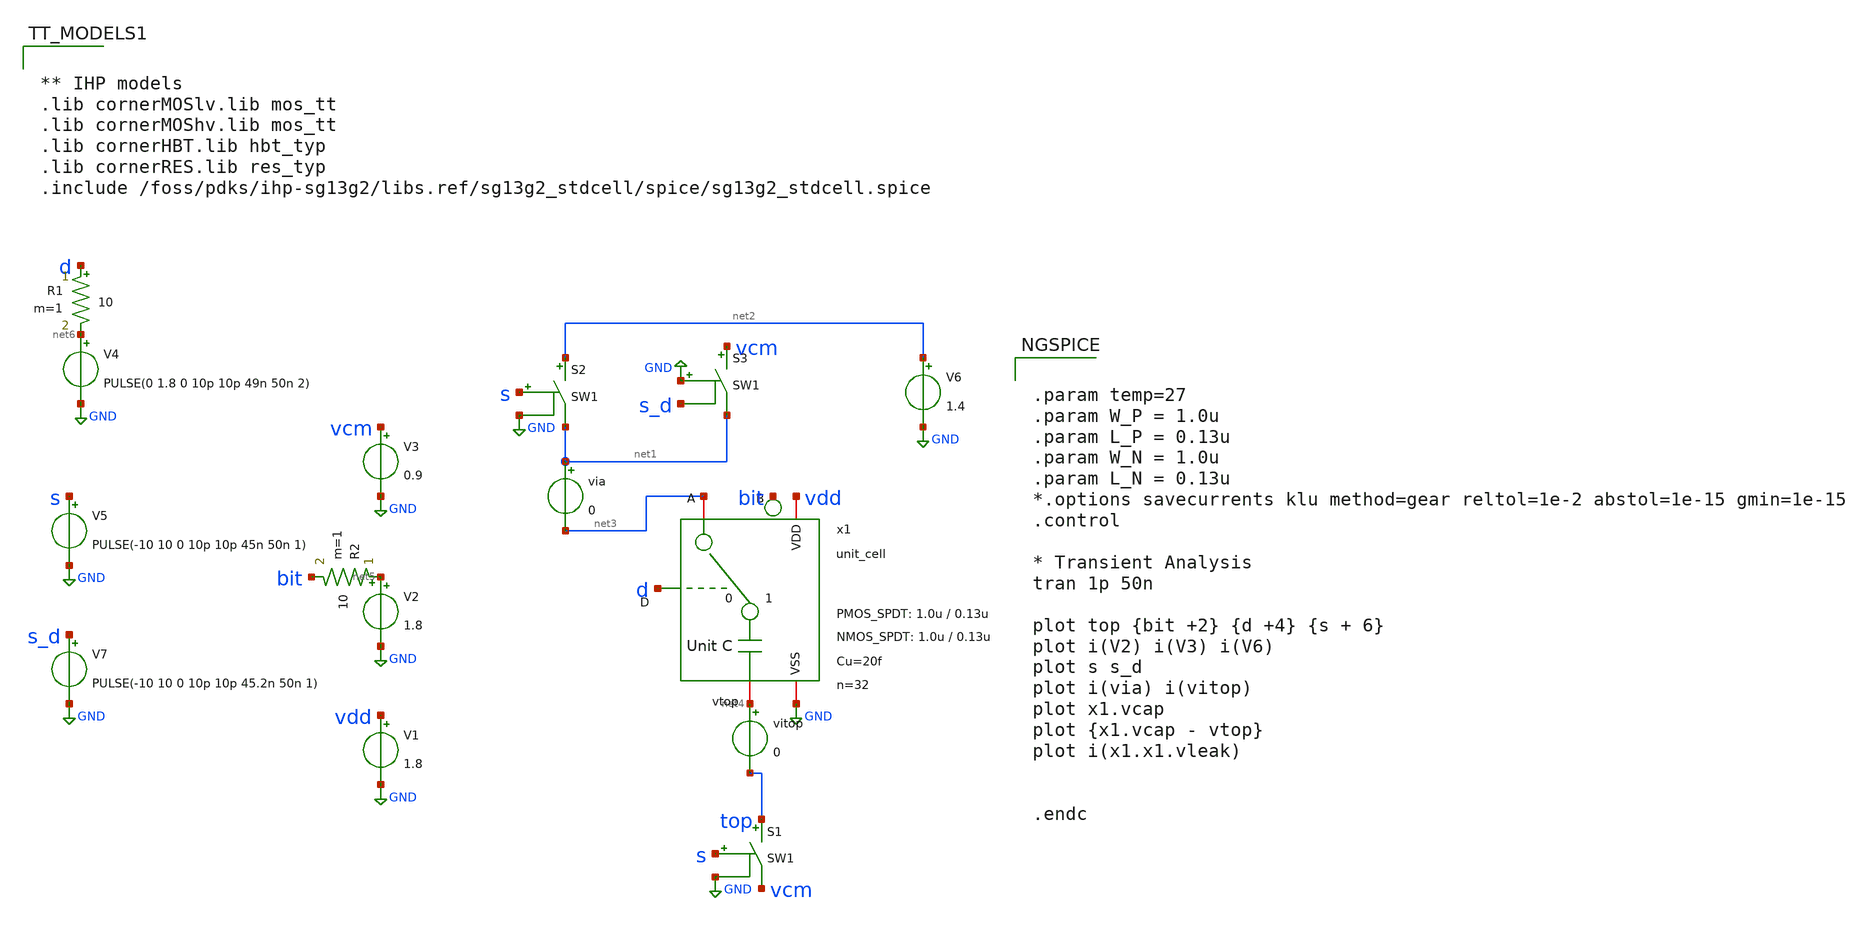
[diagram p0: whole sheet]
** sch_path: xschem/dac_icms_cell/testbenches/tb_unit_cell_tran.sch
**.subckt tb_unit_cell_tran
x1 bit net3 GND d vdd net4 unit_cell W_P_SPDT=1.0u L_P_SPDT=0.13u W_N_SPDT=1.0u L_N_SPDT=0.13u
+ Cu=20f n=32
V1 vdd GND 1.8
V2 net5 GND 1.8
V3 vcm GND 0.9
V4 net6 GND PULSE(0 1.8 0 10p 10p 49n 50n 2)
S1 top vcm s GND SW1
V5 s GND PULSE(-10 10 0 10p 10p 45n 50n 1)
S2 net2 net1 s GND SW1
S3 vcm net1 GND s_d SW1
V6 net2 GND 1.4
V7 s_d GND PULSE(-10 10 0 10p 10p 45.2n 50n 1)
via net1 net3 0
vitop net4 top 0
R1 d net6 10 m=1
R2 net5 bit 10 m=1
**** begin user architecture code


.param temp=27
.param W_P = 1.0u
.param L_P = 0.13u
.param W_N = 1.0u
.param L_N = 0.13u
*.options savecurrents klu method=gear reltol=1e-2 abstol=1e-15 gmin=1e-15
.control

* Transient Analysis
tran 1p 50n

plot top {bit +2} {d +4} {s + 6}
plot i(V2) i(V3) i(V6)
plot s s_d
plot i(via) i(vitop)
plot x1.vcap
plot {x1.vcap - vtop}
plot i(x1.x1.vleak)


.endc




** IHP models
.lib cornerMOSlv.lib mos_tt
.lib cornerMOShv.lib mos_tt
.lib cornerHBT.lib hbt_typ
.lib cornerRES.lib res_typ
.include /foss/pdks/ihp-sg13g2/libs.ref/sg13g2_stdcell/spice/sg13g2_stdcell.spice


**** end user architecture code
**.ends

* expanding   symbol:  dac_icms_cell/unit_cell.sym # of pins=6
** sym_path: xschem/dac_icms_cell/unit_cell.sym
** sch_path: xschem/dac_icms_cell/unit_cell.sch
.subckt unit_cell B A VSS D VDD vtop  W_P_SPDT=1.0u L_P_SPDT=0.13u W_N_SPDT=1.0u L_N_SPDT=0.13u
+ Cu=8f n=1
*.iopin VSS
*.iopin A
*.iopin VDD
*.ipin D
*.iopin B
*.iopin vtop
x1 VDD D VSS vcap B A dac_switch W_P_TG=3.0u L_P_TG=0.13u W_N_TG=1.0u L_N_TG=0.13u n=n
C1 vcap vtop Cu m=n
.ends


* expanding   symbol:  dac_icms_cell/dac_switch.sym # of pins=6
** sym_path: xschem/dac_icms_cell/dac_switch.sym
** sch_path: xschem/dac_icms_cell/dac_switch.sch
.subckt dac_switch VDD di_spdt_ctrl VSS v_c v_b v_a  W_P_TG=3.0u L_P_TG=0.13u W_N_TG=1.0u
+ L_N_TG=0.13u n=1
*.iopin v_a
*.iopin v_c
*.iopin VDD
*.iopin VSS
*.ipin di_spdt_ctrl
*.iopin v_b
x1 VDD di_spdt_ctrl VSS net2 v_a di_spdt_ctrl_n transmission_gate_lv_w_dummy W_P=W_P_TG L_P=L_P_TG
+ W_N=W_N_TG L_N=L_N_TG W_P_D=1.0u L_P_D=0.13u W_N_D=1.0u L_N_D=0.13u n=n
x8 VDD di_spdt_ctrl di_spdt_ctrl_n VSS inverter_lv W_P=W_P_TG L_P=L_P_TG W_N=W_N_TG L_N=L_N_TG N_C=1
XM1 net1 v_b VSS VSS sg13_lv_nmos w=0.5u l=0.2u ng=1 m=n mm_ok=1
XM3 net1 v_b VDD VDD sg13_lv_pmos w=1u l=0.2u ng=1 m=n mm_ok=1
x2 VDD di_spdt_ctrl_n VSS net3 net1 di_spdt_ctrl transmission_gate_lv_w_dummy W_P=W_P_TG L_P=L_P_TG
+ W_N=W_N_TG L_N=L_N_TG W_P_D=1.0u L_P_D=0.13u W_N_D=1.0u L_N_D=0.13u n=n
V1 v_c net2 0
V2 v_c net3 0
.ends


* expanding   symbol:  transmission_gate/transmission_gate_lv_w_dummy.sym # of pins=6
** sym_path: xschem/transmission_gate/transmission_gate_lv_w_dummy.sym
** sch_path: xschem/transmission_gate/transmission_gate_lv_w_dummy.sch
.subckt transmission_gate_lv_w_dummy VDD di_tg_ctrl VSS v_b v_a di_tg_ctrl_n  W_P=2.0u L_P=0.13u
+ W_N=2.0u L_N=0.13u W_P_D=1.0u L_P_D=0.13u W_N_D=1.0u L_N_D=0.13u n=1
*.iopin v_a
*.iopin v_b
*.iopin VDD
*.iopin VSS
*.ipin di_tg_ctrl
*.ipin di_tg_ctrl_n
XM1 v_a di_tg_ctrl v_b VSS sg13_lv_nmos w=W_N l=L_N ng=1 m=n mm_ok=1
XM2 v_a di_tg_ctrl_n v_b VDD sg13_lv_pmos w=W_P l=L_P ng=1 m=n mm_ok=1
XMdummy2 v_b di_tg_ctrl v_b VDD sg13_lv_pmos w=W_P l=L_P ng=1 m={n/2} mm_ok=1
XMdummy1 v_b di_tg_ctrl_n v_b VSS sg13_lv_nmos w=W_N l=L_N ng=1 m={n/2} mm_ok=1
.ends


* expanding   symbol:  inverter/inverter_lv.sym # of pins=4
** sym_path: xschem/inverter/inverter_lv.sym
** sch_path: xschem/inverter/inverter_lv.sch
.subckt inverter_lv VDD vin vout VSS  W_P=3.0u L_P=0.13u W_N=1.0u L_N=0.13u N_C=1
*.ipin vin
*.iopin VDD
*.iopin VSS
*.opin vout
XM1 vout vin VDD VDD sg13_lv_pmos w=W_P l=L_P ng=1 m={N_C} mm_ok=1
XM2 vout vin VSS VSS sg13_lv_nmos w=W_N l=L_N ng=1 m={N_C} mm_ok=1
.ends

.GLOBAL GND
**** begin user architecture code
.MODEL SW1 SW   VT=0.9 VH=0.01  RON=10 ROFF=1G
**** end user architecture code
.end
